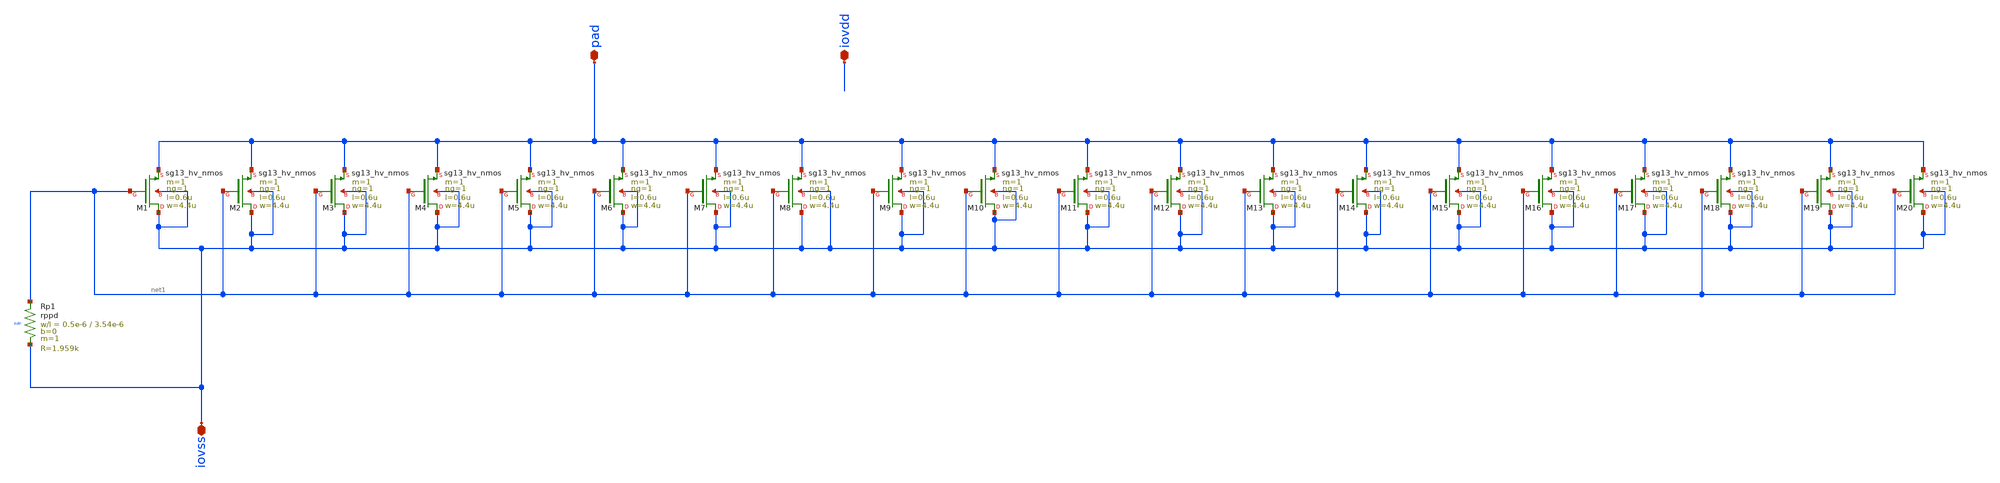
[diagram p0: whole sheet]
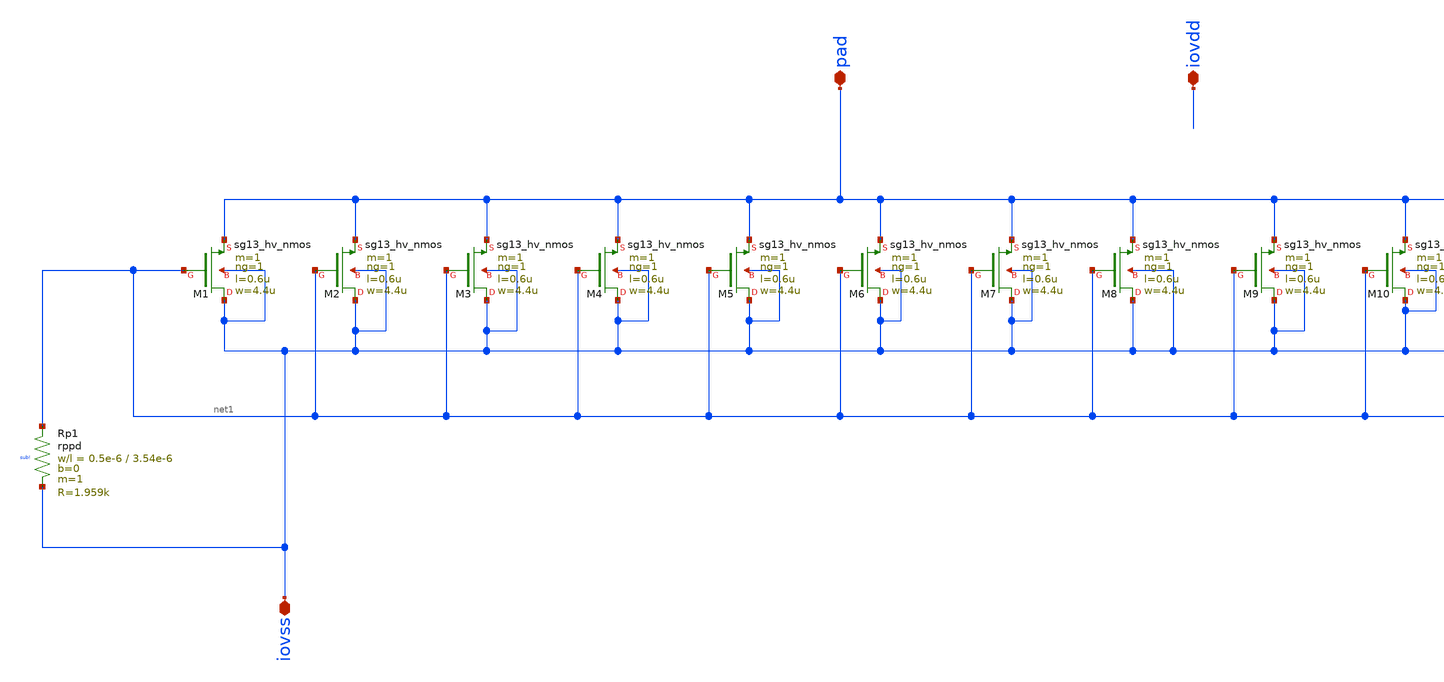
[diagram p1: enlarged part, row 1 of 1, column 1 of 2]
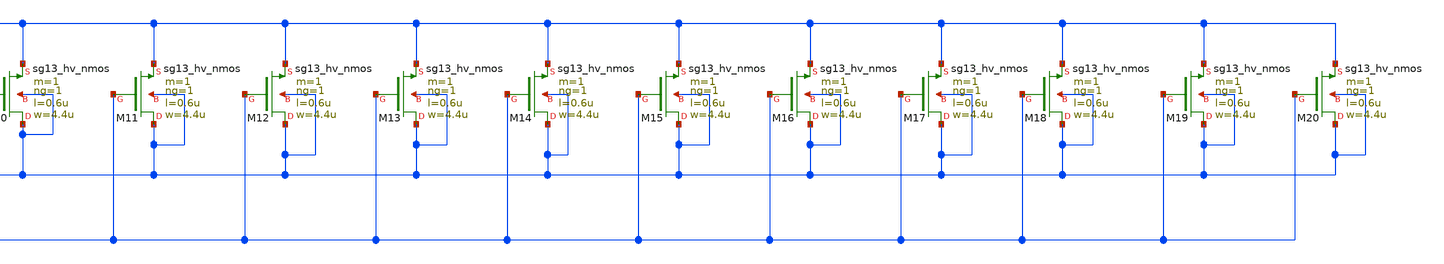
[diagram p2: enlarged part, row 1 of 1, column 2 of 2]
** sch_path: ihp-sg13g2/libs.ref/sg13g2_io/xschem/sg13g2_Clamp_N20N0D.sch
**.subckt sg13g2_Clamp_N20N0D iovss pad iovdd
*.iopin iovss
*.iopin pad
*.iopin iovdd
XM1 iovss net1 pad iovss sg13_hv_nmos w=4.4u l=0.6u ng=1 m=1 mm_ok=1
XM2 iovss net1 pad iovss sg13_hv_nmos w=4.4u l=0.6u ng=1 m=1 mm_ok=1
XM3 iovss net1 pad iovss sg13_hv_nmos w=4.4u l=0.6u ng=1 m=1 mm_ok=1
XM4 iovss net1 pad iovss sg13_hv_nmos w=4.4u l=0.6u ng=1 m=1 mm_ok=1
XM5 iovss net1 pad iovss sg13_hv_nmos w=4.4u l=0.6u ng=1 m=1 mm_ok=1
XM6 iovss net1 pad iovss sg13_hv_nmos w=4.4u l=0.6u ng=1 m=1 mm_ok=1
XM7 iovss net1 pad iovss sg13_hv_nmos w=4.4u l=0.6u ng=1 m=1 mm_ok=1
XM8 iovss net1 pad iovss sg13_hv_nmos w=4.4u l=0.6u ng=1 m=1 mm_ok=1
XM9 iovss net1 pad iovss sg13_hv_nmos w=4.4u l=0.6u ng=1 m=1 mm_ok=1
XM10 iovss net1 pad iovss sg13_hv_nmos w=4.4u l=0.6u ng=1 m=1 mm_ok=1
XM11 iovss net1 pad iovss sg13_hv_nmos w=4.4u l=0.6u ng=1 m=1 mm_ok=1
XM12 iovss net1 pad iovss sg13_hv_nmos w=4.4u l=0.6u ng=1 m=1 mm_ok=1
XM13 iovss net1 pad iovss sg13_hv_nmos w=4.4u l=0.6u ng=1 m=1 mm_ok=1
XM14 iovss net1 pad iovss sg13_hv_nmos w=4.4u l=0.6u ng=1 m=1 mm_ok=1
XM15 iovss net1 pad iovss sg13_hv_nmos w=4.4u l=0.6u ng=1 m=1 mm_ok=1
XM16 iovss net1 pad iovss sg13_hv_nmos w=4.4u l=0.6u ng=1 m=1 mm_ok=1
XM17 iovss net1 pad iovss sg13_hv_nmos w=4.4u l=0.6u ng=1 m=1 mm_ok=1
XM18 iovss net1 pad iovss sg13_hv_nmos w=4.4u l=0.6u ng=1 m=1 mm_ok=1
XM19 iovss net1 pad iovss sg13_hv_nmos w=4.4u l=0.6u ng=1 m=1 mm_ok=1
XM20 iovss net1 pad iovss sg13_hv_nmos w=4.4u l=0.6u ng=1 m=1 mm_ok=1
XRp1 net1 iovss sub! rppd w=0.5e-6 l=3.54e-6 m=1 b=0 mm_ok=1
**.ends
.end
